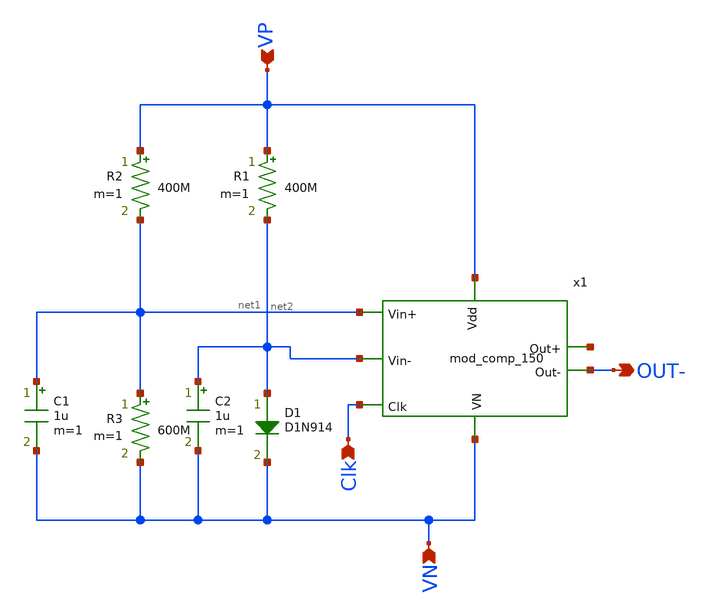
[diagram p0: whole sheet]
** sch_path: Blocks/Output_monitor/output_monitor.sch
**.subckt output_monitor Clk VP VN OUT-
*.ipin Clk
*.ipin VP
*.ipin VN
*.opin OUT-
R1 VP net2 400M m=1
R2 VP net1 400M m=1
R3 net1 VN 600M m=1
D1 net2 VN D1N914 area=1
C1 net1 VN 1u m=1
C2 net2 VN 1u m=1
x1 net2 net1 VP VN Clk net3 OUT- mod_comp_150
**.ends

* expanding   symbol:  Blocks/comparator_150nm/mod_comp_150.sym # of pins=7
** sym_path: Blocks/comparator_150nm/mod_comp_150.sym
** sch_path: Blocks/comparator_150nm/mod_comp_150.sch
.subckt mod_comp_150 Vin- Vin+ Vdd VN Clk Out+ Out-
*.ipin Vin-
*.ipin Vin+
*.ipin Vdd
*.ipin VN
*.ipin Clk
*.opin Out+
*.opin Out-
XM6 net1 Clkb1 Vdd Vdd sky130_fd_pr__pfet_01v8 L=0.15 W=1.26 nf=1 ad='int((nf+1)/2) * W/nf * 0.29' as='int((nf+2)/2) * W/nf * 0.29'
+ pd='2*int((nf+1)/2) * (W/nf + 0.29)' ps='2*int((nf+2)/2) * (W/nf + 0.29)' nrd='0.29 / W' nrs='0.29 / W'
+ sa=0 sb=0 sd=0 mult=1 m=1
XM7 O1- Vin+ net1 Vdd sky130_fd_pr__pfet_01v8 L=0.15 W=1.26 nf=1 ad='int((nf+1)/2) * W/nf * 0.29' as='int((nf+2)/2) * W/nf * 0.29'
+ pd='2*int((nf+1)/2) * (W/nf + 0.29)' ps='2*int((nf+2)/2) * (W/nf + 0.29)' nrd='0.29 / W' nrs='0.29 / W'
+ sa=0 sb=0 sd=0 mult=1 m=1
XM8 O1+ Vin- net1 Vdd sky130_fd_pr__pfet_01v8 L=0.15 W=1.26 nf=1 ad='int((nf+1)/2) * W/nf * 0.29' as='int((nf+2)/2) * W/nf * 0.29'
+ pd='2*int((nf+1)/2) * (W/nf + 0.29)' ps='2*int((nf+2)/2) * (W/nf + 0.29)' nrd='0.29 / W' nrs='0.29 / W'
+ sa=0 sb=0 sd=0 mult=1 m=1
XM9 net5 Clkb2 Vdd Vdd sky130_fd_pr__pfet_01v8 L=0.15 W=1.26 nf=1 ad='int((nf+1)/2) * W/nf * 0.29' as='int((nf+2)/2) * W/nf * 0.29'
+ pd='2*int((nf+1)/2) * (W/nf + 0.29)' ps='2*int((nf+2)/2) * (W/nf + 0.29)' nrd='0.29 / W' nrs='0.29 / W'
+ sa=0 sb=0 sd=0 mult=1 m=1
XM10 net7 O2- net5 Vdd sky130_fd_pr__pfet_01v8 L=0.15 W=1.26 nf=1 ad='int((nf+1)/2) * W/nf * 0.29' as='int((nf+2)/2) * W/nf * 0.29'
+ pd='2*int((nf+1)/2) * (W/nf + 0.29)' ps='2*int((nf+2)/2) * (W/nf + 0.29)' nrd='0.29 / W' nrs='0.29 / W'
+ sa=0 sb=0 sd=0 mult=1 m=1
XM11 O2- O1- net6 Vdd sky130_fd_pr__pfet_01v8 L=0.15 W=1.26 nf=1 ad='int((nf+1)/2) * W/nf * 0.29' as='int((nf+2)/2) * W/nf * 0.29'
+ pd='2*int((nf+1)/2) * (W/nf + 0.29)' ps='2*int((nf+2)/2) * (W/nf + 0.29)' nrd='0.29 / W' nrs='0.29 / W'
+ sa=0 sb=0 sd=0 mult=1 m=1
XM12 O2+ O1+ net7 Vdd sky130_fd_pr__pfet_01v8 L=0.15 W=1.26 nf=1 ad='int((nf+1)/2) * W/nf * 0.29' as='int((nf+2)/2) * W/nf * 0.29'
+ pd='2*int((nf+1)/2) * (W/nf + 0.29)' ps='2*int((nf+2)/2) * (W/nf + 0.29)' nrd='0.29 / W' nrs='0.29 / W'
+ sa=0 sb=0 sd=0 mult=1 m=1
XM13 net6 O2+ net5 Vdd sky130_fd_pr__pfet_01v8 L=0.15 W=1.26 nf=1 ad='int((nf+1)/2) * W/nf * 0.29' as='int((nf+2)/2) * W/nf * 0.29'
+ pd='2*int((nf+1)/2) * (W/nf + 0.29)' ps='2*int((nf+2)/2) * (W/nf + 0.29)' nrd='0.29 / W' nrs='0.29 / W'
+ sa=0 sb=0 sd=0 mult=1 m=1
XM1 O1+ O1- net2 VN sky130_fd_pr__nfet_01v8 L=0.15 W=0.42 nf=1 ad='int((nf+1)/2) * W/nf * 0.29' as='int((nf+2)/2) * W/nf * 0.29'
+ pd='2*int((nf+1)/2) * (W/nf + 0.29)' ps='2*int((nf+2)/2) * (W/nf + 0.29)' nrd='0.29 / W' nrs='0.29 / W'
+ sa=0 sb=0 sd=0 mult=1 m=1
XM3 net2 Vdd VN VN sky130_fd_pr__nfet_01v8 L=0.15 W=0.42 nf=1 ad='int((nf+1)/2) * W/nf * 0.29' as='int((nf+2)/2) * W/nf * 0.29'
+ pd='2*int((nf+1)/2) * (W/nf + 0.29)' ps='2*int((nf+2)/2) * (W/nf + 0.29)' nrd='0.29 / W' nrs='0.29 / W'
+ sa=0 sb=0 sd=0 mult=1 m=1
XM4 O1- O1+ net2 VN sky130_fd_pr__nfet_01v8 L=0.15 W=0.42 nf=1 ad='int((nf+1)/2) * W/nf * 0.29' as='int((nf+2)/2) * W/nf * 0.29'
+ pd='2*int((nf+1)/2) * (W/nf + 0.29)' ps='2*int((nf+2)/2) * (W/nf + 0.29)' nrd='0.29 / W' nrs='0.29 / W'
+ sa=0 sb=0 sd=0 mult=1 m=1
XM5 O1- Clk VN VN sky130_fd_pr__nfet_01v8 L=0.15 W=0.42 nf=1 ad='int((nf+1)/2) * W/nf * 0.29' as='int((nf+2)/2) * W/nf * 0.29'
+ pd='2*int((nf+1)/2) * (W/nf + 0.29)' ps='2*int((nf+2)/2) * (W/nf + 0.29)' nrd='0.29 / W' nrs='0.29 / W'
+ sa=0 sb=0 sd=0 mult=1 m=1
XM21 O1+ Clk VN VN sky130_fd_pr__nfet_01v8 L=0.15 W=0.42 nf=1 ad='int((nf+1)/2) * W/nf * 0.29' as='int((nf+2)/2) * W/nf * 0.29'
+ pd='2*int((nf+1)/2) * (W/nf + 0.29)' ps='2*int((nf+2)/2) * (W/nf + 0.29)' nrd='0.29 / W' nrs='0.29 / W'
+ sa=0 sb=0 sd=0 mult=1 m=1
XM2 O2- O2+ VN VN sky130_fd_pr__nfet_01v8 L=0.15 W=0.42 nf=1 ad='int((nf+1)/2) * W/nf * 0.29' as='int((nf+2)/2) * W/nf * 0.29'
+ pd='2*int((nf+1)/2) * (W/nf + 0.29)' ps='2*int((nf+2)/2) * (W/nf + 0.29)' nrd='0.29 / W' nrs='0.29 / W'
+ sa=0 sb=0 sd=0 mult=1 m=1
XM14 O2+ Clk VN VN sky130_fd_pr__nfet_01v8 L=0.15 W=0.42 nf=1 ad='int((nf+1)/2) * W/nf * 0.29' as='int((nf+2)/2) * W/nf * 0.29'
+ pd='2*int((nf+1)/2) * (W/nf + 0.29)' ps='2*int((nf+2)/2) * (W/nf + 0.29)' nrd='0.29 / W' nrs='0.29 / W'
+ sa=0 sb=0 sd=0 mult=1 m=1
XM15 O2+ O2- VN VN sky130_fd_pr__nfet_01v8 L=0.15 W=0.42 nf=1 ad='int((nf+1)/2) * W/nf * 0.29' as='int((nf+2)/2) * W/nf * 0.29'
+ pd='2*int((nf+1)/2) * (W/nf + 0.29)' ps='2*int((nf+2)/2) * (W/nf + 0.29)' nrd='0.29 / W' nrs='0.29 / W'
+ sa=0 sb=0 sd=0 mult=1 m=1
XM16 O2- Clk VN VN sky130_fd_pr__nfet_01v8 L=0.15 W=0.42 nf=1 ad='int((nf+1)/2) * W/nf * 0.29' as='int((nf+2)/2) * W/nf * 0.29'
+ pd='2*int((nf+1)/2) * (W/nf + 0.29)' ps='2*int((nf+2)/2) * (W/nf + 0.29)' nrd='0.29 / W' nrs='0.29 / W'
+ sa=0 sb=0 sd=0 mult=1 m=1
XM17 net8 Clk VN VN sky130_fd_pr__nfet_01v8 L=0.15 W=0.42 nf=1 ad='int((nf+1)/2) * W/nf * 0.29' as='int((nf+2)/2) * W/nf * 0.29'
+ pd='2*int((nf+1)/2) * (W/nf + 0.29)' ps='2*int((nf+2)/2) * (W/nf + 0.29)' nrd='0.29 / W' nrs='0.29 / W'
+ sa=0 sb=0 sd=0 mult=1 m=1
XM18 net8 inv VN VN sky130_fd_pr__nfet_01v8 L=0.15 W=0.42 nf=1 ad='int((nf+1)/2) * W/nf * 0.29' as='int((nf+2)/2) * W/nf * 0.29'
+ pd='2*int((nf+1)/2) * (W/nf + 0.29)' ps='2*int((nf+2)/2) * (W/nf + 0.29)' nrd='0.29 / W' nrs='0.29 / W'
+ sa=0 sb=0 sd=0 mult=1 m=1
XM19 net9 inv Vdd Vdd sky130_fd_pr__pfet_01v8 L=0.15 W=1.26 nf=1 ad='int((nf+1)/2) * W/nf * 0.29' as='int((nf+2)/2) * W/nf * 0.29'
+ pd='2*int((nf+1)/2) * (W/nf + 0.29)' ps='2*int((nf+2)/2) * (W/nf + 0.29)' nrd='0.29 / W' nrs='0.29 / W'
+ sa=0 sb=0 sd=0 mult=1 m=1
XM22 net8 Clk net9 Vdd sky130_fd_pr__pfet_01v8 L=0.15 W=1.26 nf=1 ad='int((nf+1)/2) * W/nf * 0.29' as='int((nf+2)/2) * W/nf * 0.29'
+ pd='2*int((nf+1)/2) * (W/nf + 0.29)' ps='2*int((nf+2)/2) * (W/nf + 0.29)' nrd='0.29 / W' nrs='0.29 / W'
+ sa=0 sb=0 sd=0 mult=1 m=1
x2 Clk inv Vdd VN black_inv
x7 inv net3 Vdd VN INV
x8 net3 net4 Vdd VN INV
x9 net4 Clkb2 Vdd VN INV
x16 net8 Clkb1 Vdd VN INV
C1 inv VN 5p m=1
x1 O2+ Clk Vdd VN Vdd Out+ DFF
x4 O2- Clk Vdd VN Vdd Out- DFF
.ends


* expanding   symbol:  component/black_inv_1/black_inv.sym # of pins=4
** sym_path: component/black_inv_1/black_inv.sym
** sch_path: component/black_inv_1/black_inv.sch
.subckt black_inv X Y VP VN
*.ipin X
*.opin Y
*.iopin VN
*.iopin VP
XM8 Y X VP VP sky130_fd_pr__pfet_01v8 L=.18 W=1.59 nf=1 ad='int((nf+1)/2) * W/nf * 0.29' as='int((nf+2)/2) * W/nf * 0.29'
+ pd='2*int((nf+1)/2) * (W/nf + 0.29)' ps='2*int((nf+2)/2) * (W/nf + 0.29)' nrd='0.29 / W' nrs='0.29 / W'
+ sa=0 sb=0 sd=0 mult=1 m=1
XM4 Y X VN VN sky130_fd_pr__nfet_01v8 L=0.18 W=0.502 nf=1 ad='int((nf+1)/2) * W/nf * 0.29' as='int((nf+2)/2) * W/nf * 0.29'
+ pd='2*int((nf+1)/2) * (W/nf + 0.29)' ps='2*int((nf+2)/2) * (W/nf + 0.29)' nrd='0.29 / W' nrs='0.29 / W'
+ sa=0 sb=0 sd=0 mult=1 m=1
.ends


* expanding   symbol:  component/Inverter/INV.sym # of pins=4
** sym_path: component/Inverter/INV.sym
** sch_path: component/Inverter/INV.sch
.subckt INV X Y VP VN
*.ipin X
*.opin Y
*.iopin VN
*.iopin VP
XM8 Y X VP VP sky130_fd_pr__pfet_01v8 L=.18 W=1.512 nf=1 ad='int((nf+1)/2) * W/nf * 0.29' as='int((nf+2)/2) * W/nf * 0.29'
+ pd='2*int((nf+1)/2) * (W/nf + 0.29)' ps='2*int((nf+2)/2) * (W/nf + 0.29)' nrd='0.29 / W' nrs='0.29 / W'
+ sa=0 sb=0 sd=0 mult=1 m=1
XM4 Y X VN VN sky130_fd_pr__nfet_01v8 L=0.18 W=0.42 nf=1 ad='int((nf+1)/2) * W/nf * 0.29' as='int((nf+2)/2) * W/nf * 0.29'
+ pd='2*int((nf+1)/2) * (W/nf + 0.29)' ps='2*int((nf+2)/2) * (W/nf + 0.29)' nrd='0.29 / W' nrs='0.29 / W'
+ sa=0 sb=0 sd=0 mult=1 m=1
.ends


* expanding   symbol:  component/FlipFlops/DFF.sym # of pins=6
** sym_path: component/FlipFlops/DFF.sym
** sch_path: component/FlipFlops/DFF.sch
.subckt DFF D Clk RST VN VP Q
*.opin Q
*.iopin VN
*.iopin VP
*.ipin Clk
*.ipin D
*.ipin RST
x1 net2 net5 net4 VP VN NAND
x7 net4 Clk RST VP VN net2 NAND3
x3 Q net1 RST VP VN net3 NAND3
x4 net2 Clk net5 VP VN net1 NAND3
x5 net1 D RST VP VN net5 NAND3
x6 net3 net2 Q VP VN NAND
.ends


* expanding   symbol:  component/NAND2/NAND.sym # of pins=5
** sym_path: component/NAND2/NAND.sym
** sch_path: component/NAND2/NAND.sch
.subckt NAND B A Y VP VN
*.iopin VP
*.ipin A
*.ipin B
*.opin Y
*.iopin VN
XM1 Y A VP VP sky130_fd_pr__pfet_01v8 L=0.15 W=1.26 nf=1 ad='int((nf+1)/2) * W/nf * 0.29' as='int((nf+2)/2) * W/nf * 0.29'
+ pd='2*int((nf+1)/2) * (W/nf + 0.29)' ps='2*int((nf+2)/2) * (W/nf + 0.29)' nrd='0.29 / W' nrs='0.29 / W'
+ sa=0 sb=0 sd=0 mult=1 m=1
XM2 Y B VP VP sky130_fd_pr__pfet_01v8 L=0.15 W=1.26 nf=1 ad='int((nf+1)/2) * W/nf * 0.29' as='int((nf+2)/2) * W/nf * 0.29'
+ pd='2*int((nf+1)/2) * (W/nf + 0.29)' ps='2*int((nf+2)/2) * (W/nf + 0.29)' nrd='0.29 / W' nrs='0.29 / W'
+ sa=0 sb=0 sd=0 mult=1 m=1
XM3 Y A net1 net1 sky130_fd_pr__nfet_01v8 L=0.15 W=0.84 nf=1 ad='int((nf+1)/2) * W/nf * 0.29' as='int((nf+2)/2) * W/nf * 0.29'
+ pd='2*int((nf+1)/2) * (W/nf + 0.29)' ps='2*int((nf+2)/2) * (W/nf + 0.29)' nrd='0.29 / W' nrs='0.29 / W'
+ sa=0 sb=0 sd=0 mult=1 m=1
XM4 net1 B VN VN sky130_fd_pr__nfet_01v8 L=0.15 W=0.84 nf=1 ad='int((nf+1)/2) * W/nf * 0.29' as='int((nf+2)/2) * W/nf * 0.29'
+ pd='2*int((nf+1)/2) * (W/nf + 0.29)' ps='2*int((nf+2)/2) * (W/nf + 0.29)' nrd='0.29 / W' nrs='0.29 / W'
+ sa=0 sb=0 sd=0 mult=1 m=1
.ends


* expanding   symbol:  component/NAND3/NAND3.sym # of pins=6
** sym_path: component/NAND3/NAND3.sym
** sch_path: component/NAND3/NAND3.sch
.subckt NAND3 A B C VP VN Y
*.iopin VP
*.iopin VN
*.ipin A
*.ipin B
*.ipin C
*.opin Y
XM1 Y A net1 VN sky130_fd_pr__nfet_01v8 L=0.15 W=1.26 nf=1 ad='int((nf+1)/2) * W/nf * 0.29' as='int((nf+2)/2) * W/nf * 0.29'
+ pd='2*int((nf+1)/2) * (W/nf + 0.29)' ps='2*int((nf+2)/2) * (W/nf + 0.29)' nrd='0.29 / W' nrs='0.29 / W'
+ sa=0 sb=0 sd=0 mult=1 m=1
XM2 net1 B net2 VN sky130_fd_pr__nfet_01v8 L=0.15 W=1.26 nf=1 ad='int((nf+1)/2) * W/nf * 0.29' as='int((nf+2)/2) * W/nf * 0.29'
+ pd='2*int((nf+1)/2) * (W/nf + 0.29)' ps='2*int((nf+2)/2) * (W/nf + 0.29)' nrd='0.29 / W' nrs='0.29 / W'
+ sa=0 sb=0 sd=0 mult=1 m=1
XM3 net2 C VN VN sky130_fd_pr__nfet_01v8 L=0.15 W=1.26 nf=1 ad='int((nf+1)/2) * W/nf * 0.29' as='int((nf+2)/2) * W/nf * 0.29'
+ pd='2*int((nf+1)/2) * (W/nf + 0.29)' ps='2*int((nf+2)/2) * (W/nf + 0.29)' nrd='0.29 / W' nrs='0.29 / W'
+ sa=0 sb=0 sd=0 mult=1 m=1
XM4 Y A VP VP sky130_fd_pr__pfet_01v8 L=0.15 W=1.26 nf=1 ad='int((nf+1)/2) * W/nf * 0.29' as='int((nf+2)/2) * W/nf * 0.29'
+ pd='2*int((nf+1)/2) * (W/nf + 0.29)' ps='2*int((nf+2)/2) * (W/nf + 0.29)' nrd='0.29 / W' nrs='0.29 / W'
+ sa=0 sb=0 sd=0 mult=1 m=1
XM5 Y B VP VP sky130_fd_pr__pfet_01v8 L=0.15 W=1.26 nf=1 ad='int((nf+1)/2) * W/nf * 0.29' as='int((nf+2)/2) * W/nf * 0.29'
+ pd='2*int((nf+1)/2) * (W/nf + 0.29)' ps='2*int((nf+2)/2) * (W/nf + 0.29)' nrd='0.29 / W' nrs='0.29 / W'
+ sa=0 sb=0 sd=0 mult=1 m=1
XM6 Y C VP VP sky130_fd_pr__pfet_01v8 L=0.15 W=1.26 nf=1 ad='int((nf+1)/2) * W/nf * 0.29' as='int((nf+2)/2) * W/nf * 0.29'
+ pd='2*int((nf+1)/2) * (W/nf + 0.29)' ps='2*int((nf+2)/2) * (W/nf + 0.29)' nrd='0.29 / W' nrs='0.29 / W'
+ sa=0 sb=0 sd=0 mult=1 m=1
.ends

.end
